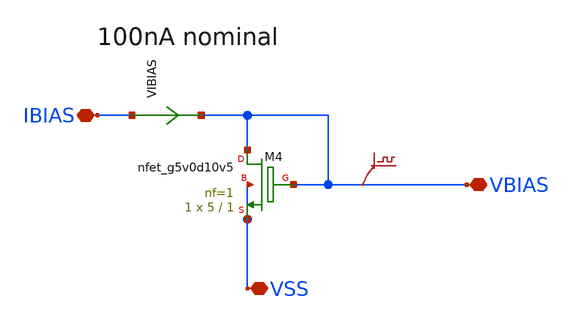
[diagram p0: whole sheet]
** sch_path: xschem/vbias_gen_pga.sch
**.subckt vbias_gen_pga VBIAS VSS IBIAS
*.iopin VBIAS
*.iopin VSS
*.iopin IBIAS
.save v(vbias)
VIBIAS IBIAS VBIAS 0
.save i(vibias)
XM4 VBIAS VBIAS VSS VSS sky130_fd_pr__nfet_g5v0d10v5 L=1 W=5 nf=1 ad='int((nf+1)/2) * W/nf * 0.29' as='int((nf+2)/2) * W/nf * 0.29'
+ pd='2*int((nf+1)/2) * (W/nf + 0.29)' ps='2*int((nf+2)/2) * (W/nf + 0.29)' nrd='0.29 / W' nrs='0.29 / W'
+ sa=0 sb=0 sd=0 mult=1 m=1
**.ends
.end
